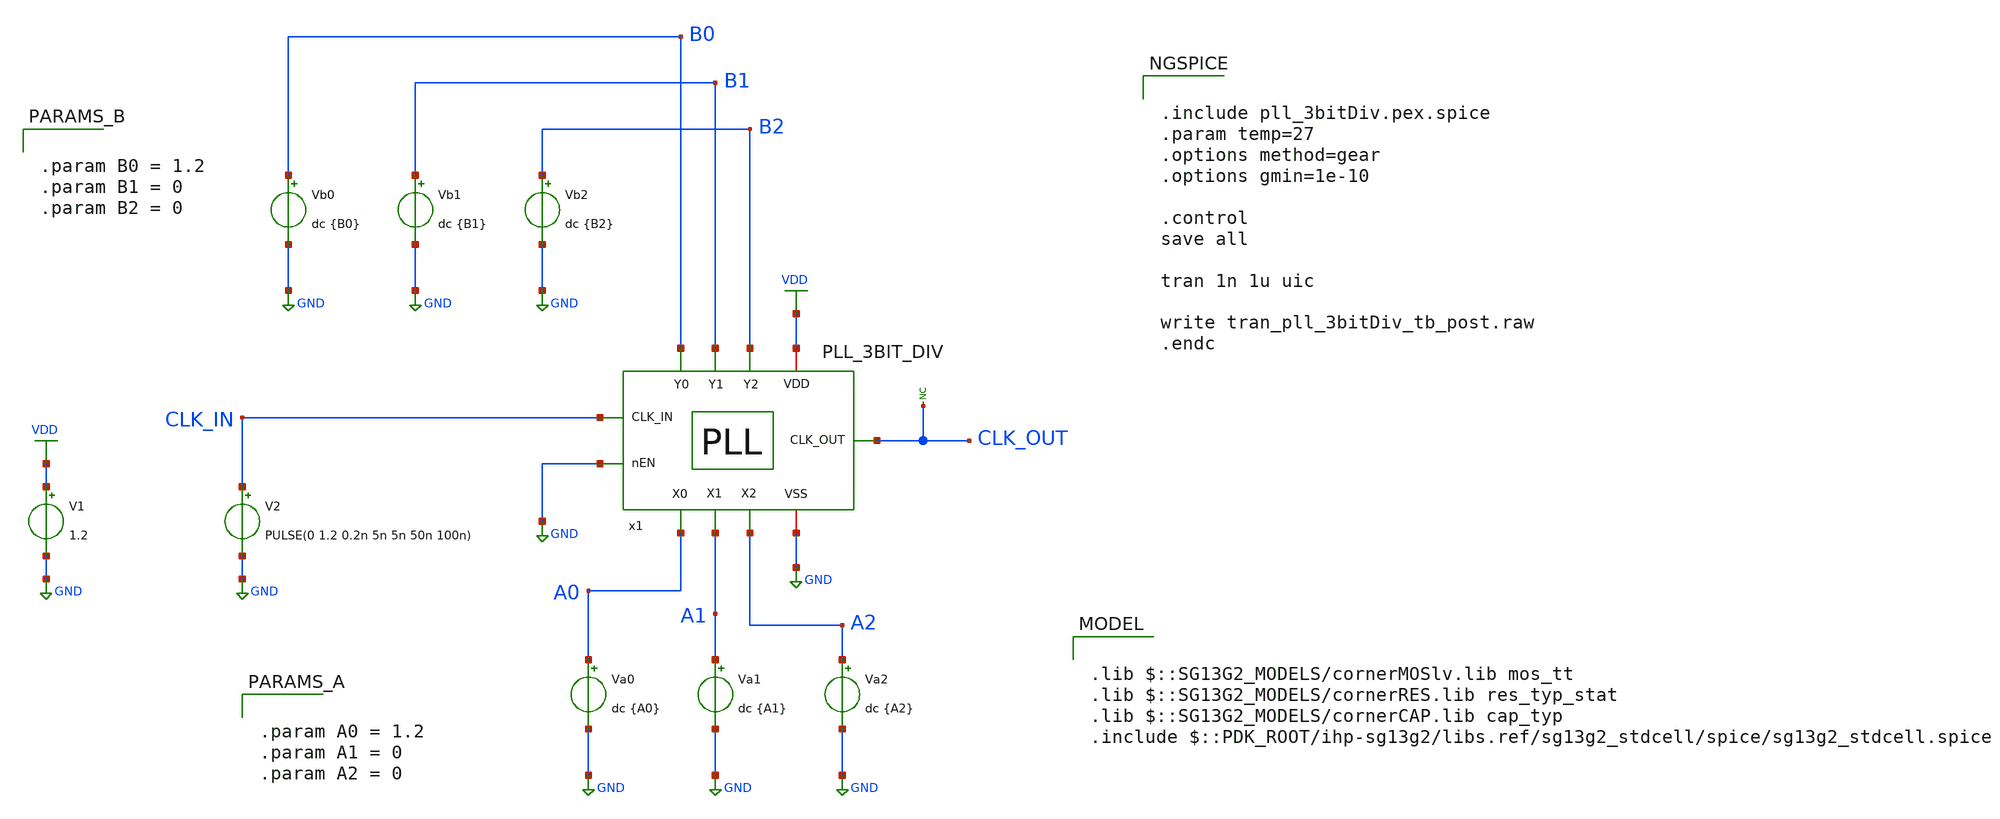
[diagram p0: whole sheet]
** sch_path: 30_MHz_Fractional_N_PLL/design_data/xschem/PLL_3BIT_DIV_TB.sch

.lib $::SG13G2_MODELS/cornerMOSlv.lib mos_tt
.lib $::SG13G2_MODELS/cornerRES.lib res_typ_stat
.lib $::SG13G2_MODELS/cornerCAP.lib cap_typ
.include $::PDK_ROOT/ihp-sg13g2/libs.ref/sg13g2_stdcell/spice/sg13g2_stdcell.spice

**.subckt PLL_3BIT_DIV_TB
V1 VDD GND 1.2
V2 CLK_IN GND PULSE(0 1.2 0.2n 5n 5n 50n 100n)
Va0 A0 GND dc {A0}
Va1 A1 GND dc {A1}
* noconn CLK_OUT
Va2 A2 GND dc {A2}
Vb0 B0 GND dc {B0}
Vb1 B1 GND dc {B1}
Vb2 B2 GND dc {B2}
x1 CLK_IN CLK_OUT B0 B2 B1 VDD GND GND A1 A2 A0 PLL_3BIT_DIV
**** begin user architecture code


.include pll_3bitDiv.pex.spice
.param temp=27
.options method=gear
.options gmin=1e-10

.control
save all

tran 1n 1u uic

write tran_pll_3bitDiv_tb_post.raw
.endc





.param A0 = 1.2
.param A1 = 0
.param A2 = 0




.param B0 = 1.2
.param B1 = 0
.param B2 = 0


**** end user architecture code
**.ends
.GLOBAL GND
.GLOBAL VDD
.end
